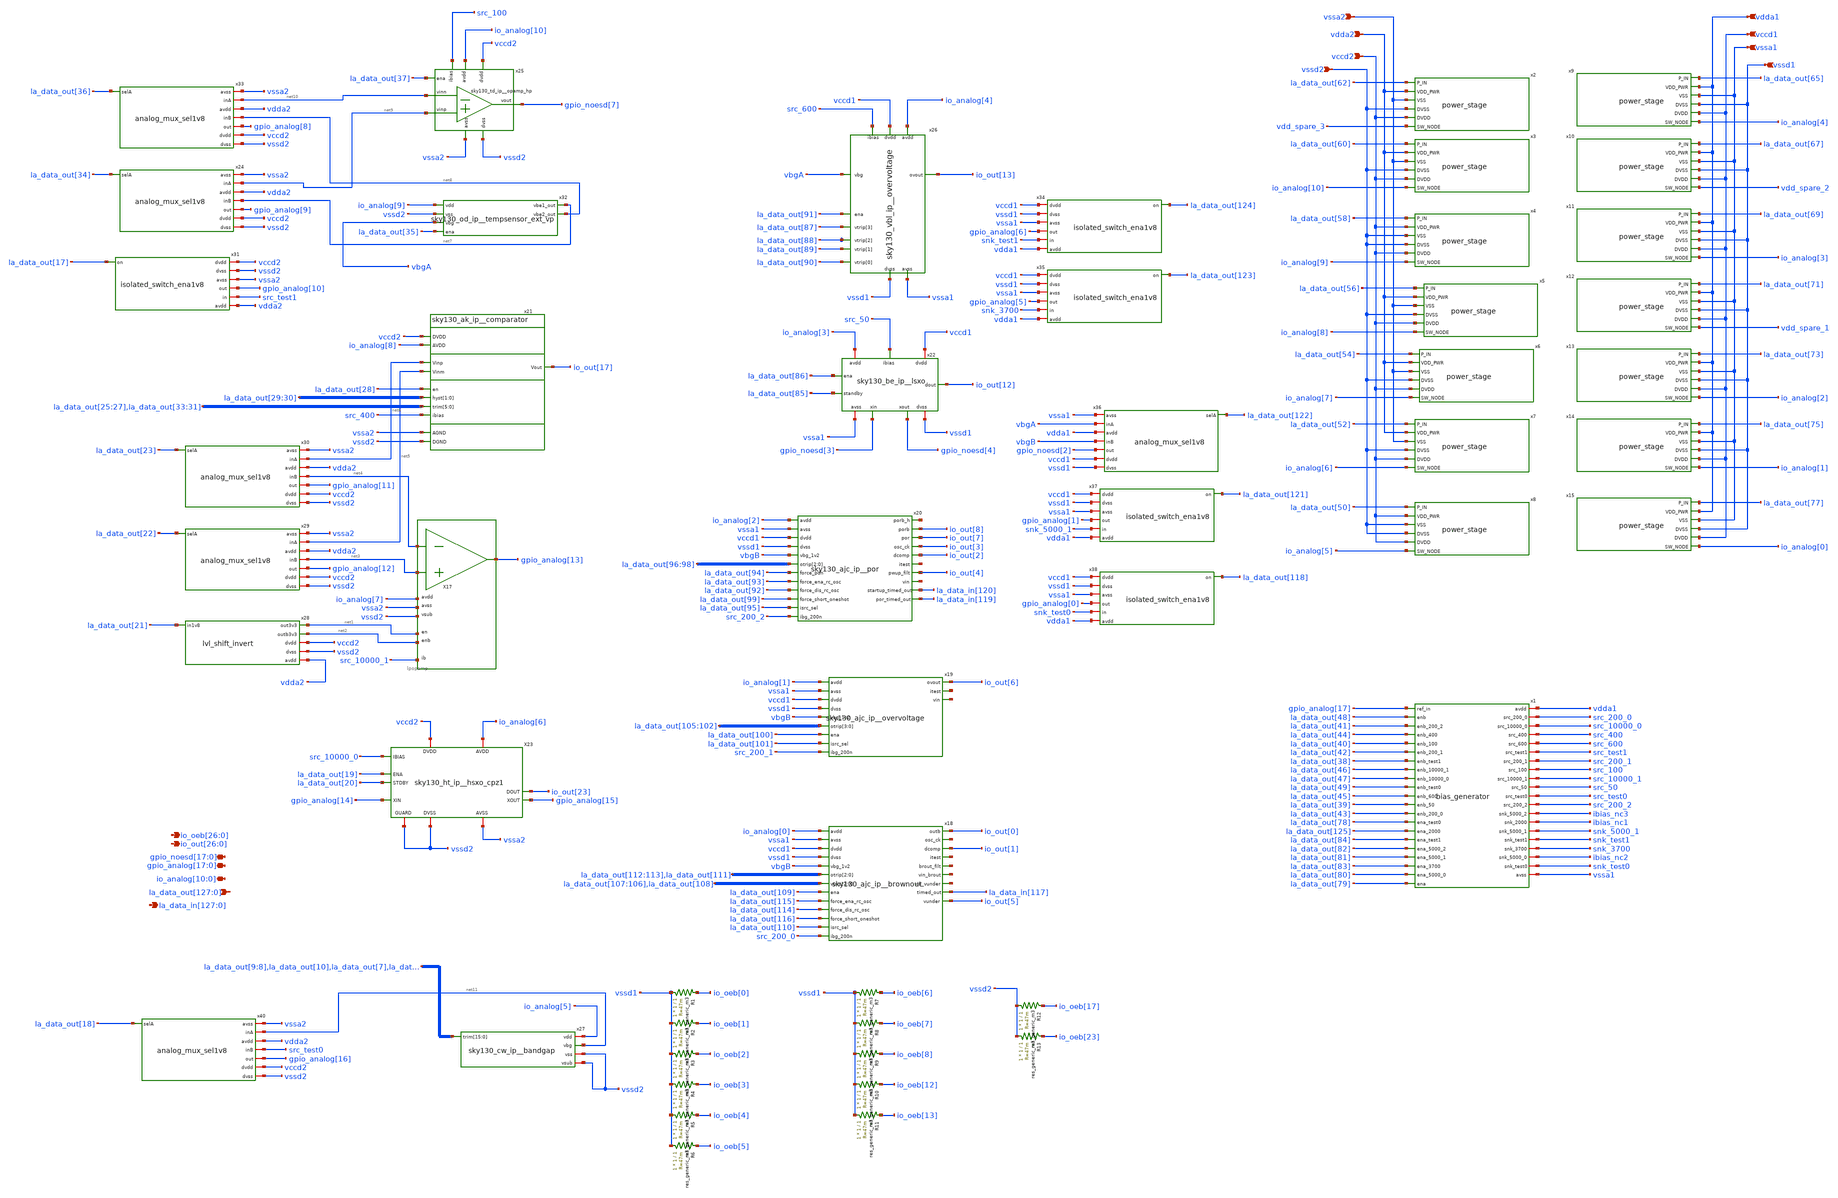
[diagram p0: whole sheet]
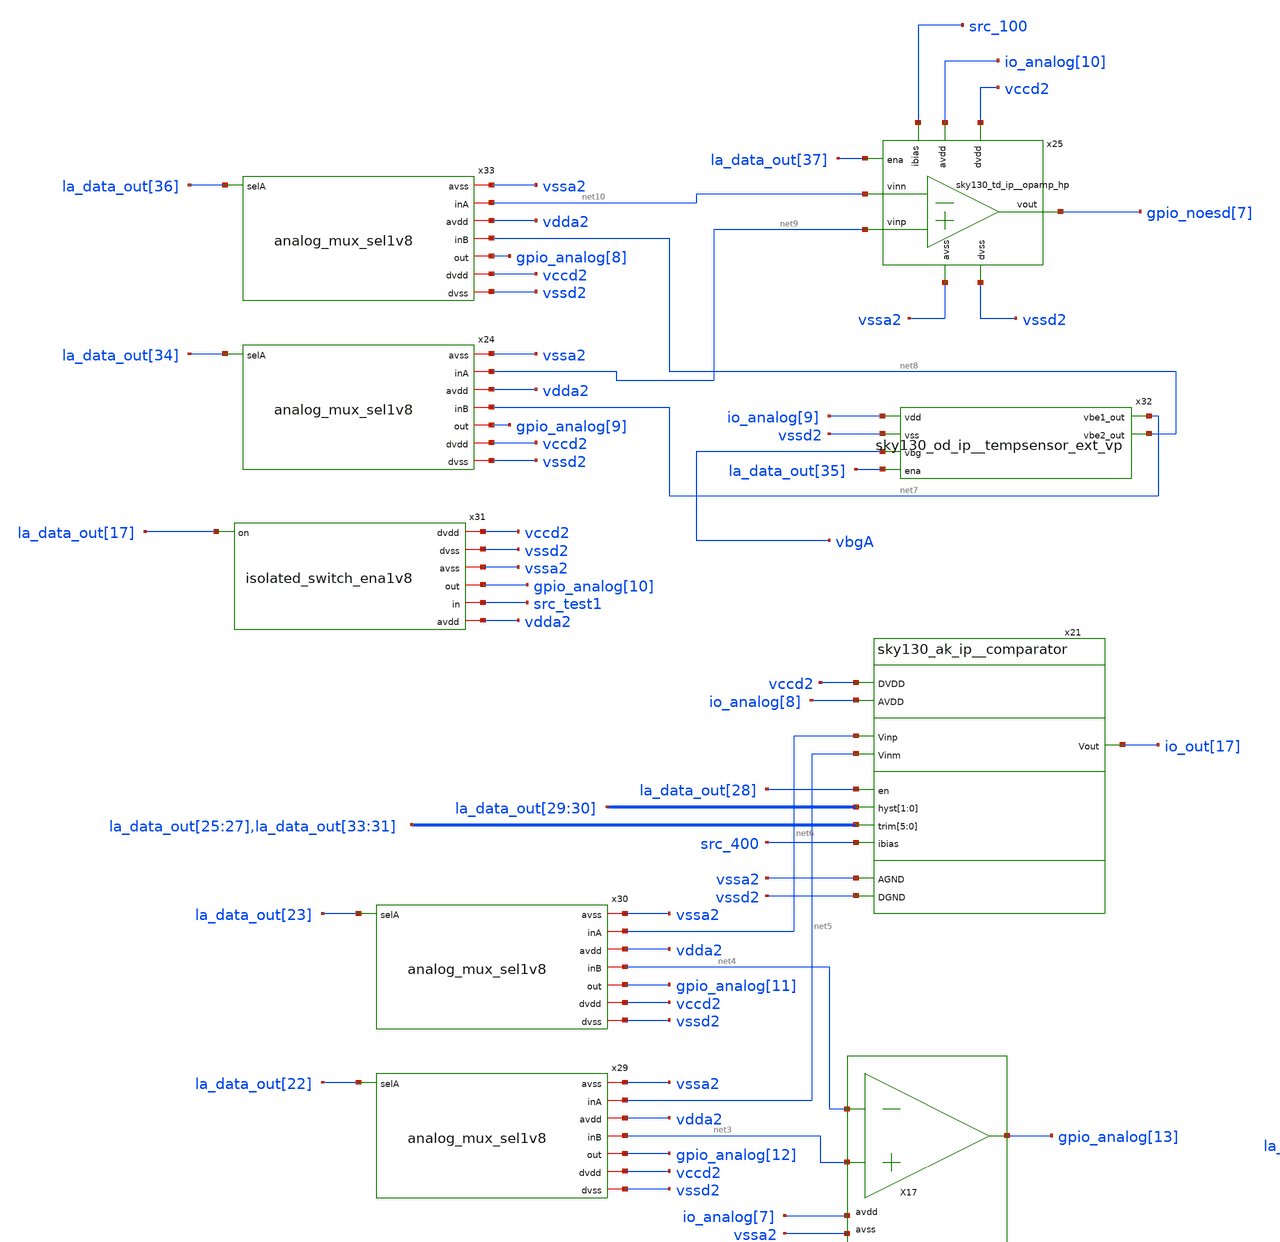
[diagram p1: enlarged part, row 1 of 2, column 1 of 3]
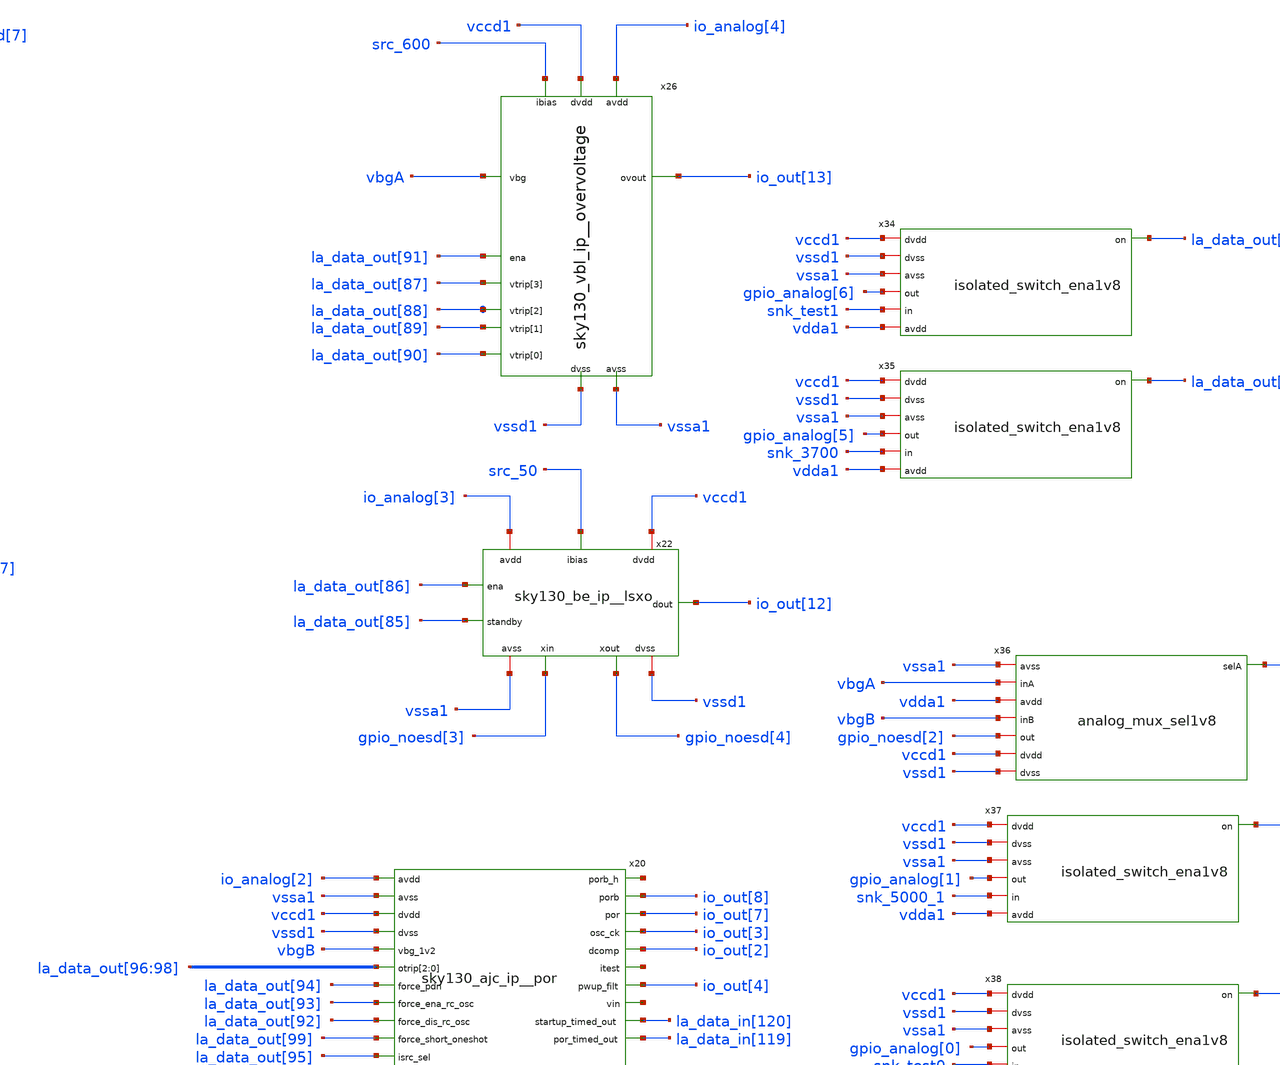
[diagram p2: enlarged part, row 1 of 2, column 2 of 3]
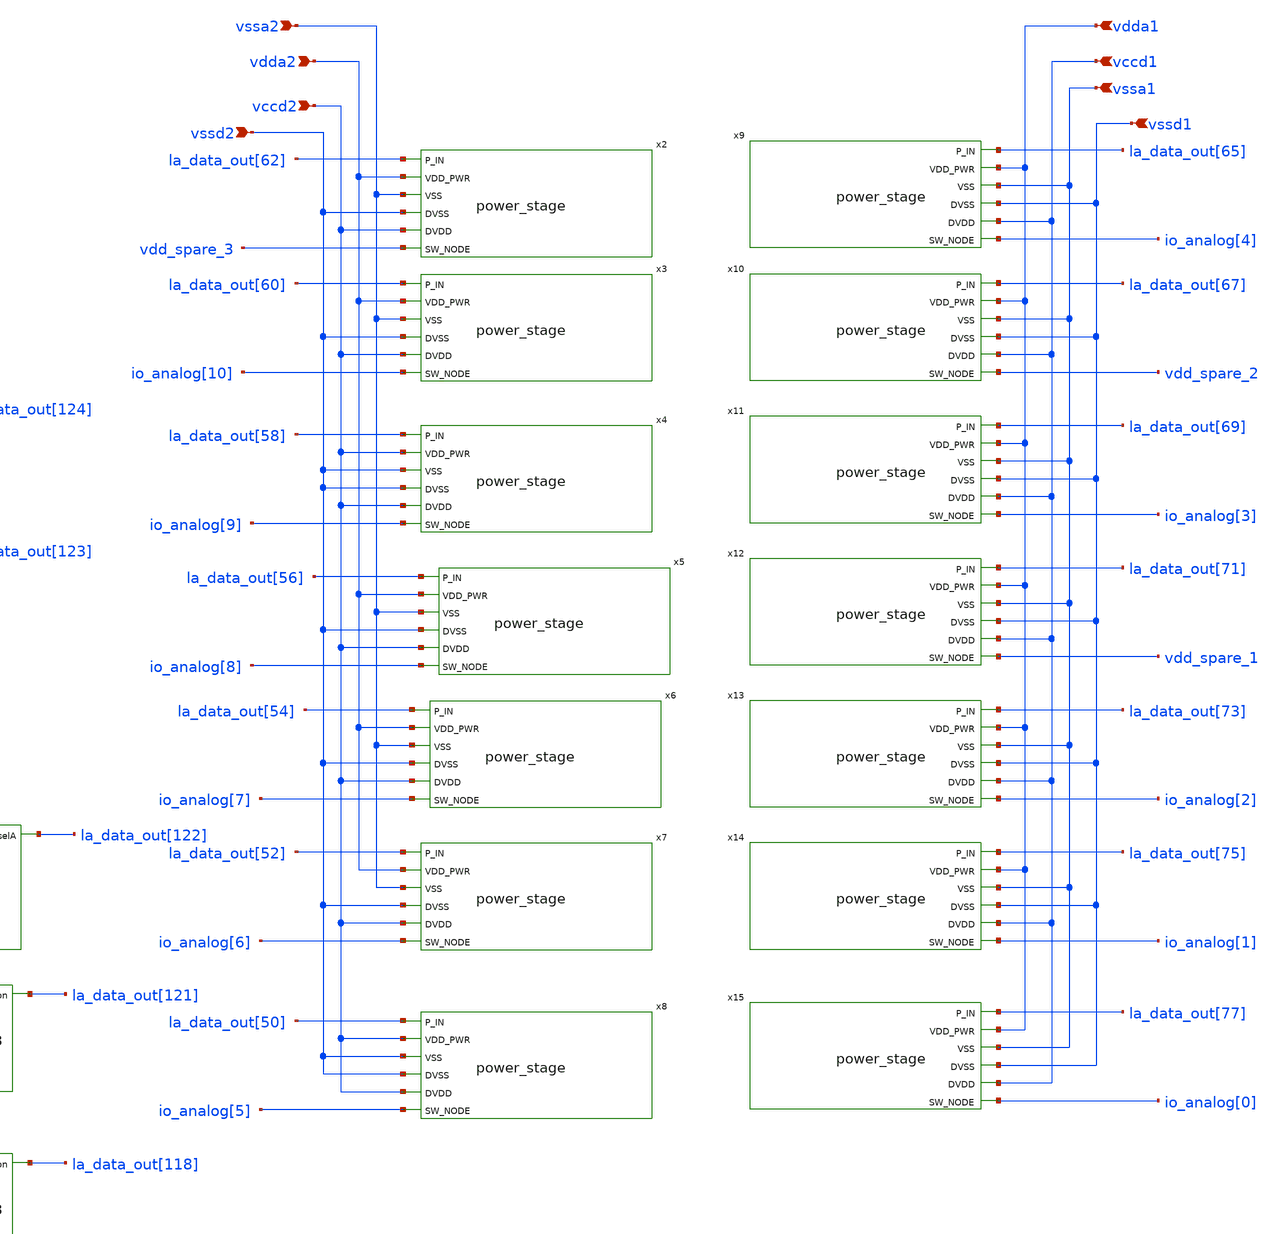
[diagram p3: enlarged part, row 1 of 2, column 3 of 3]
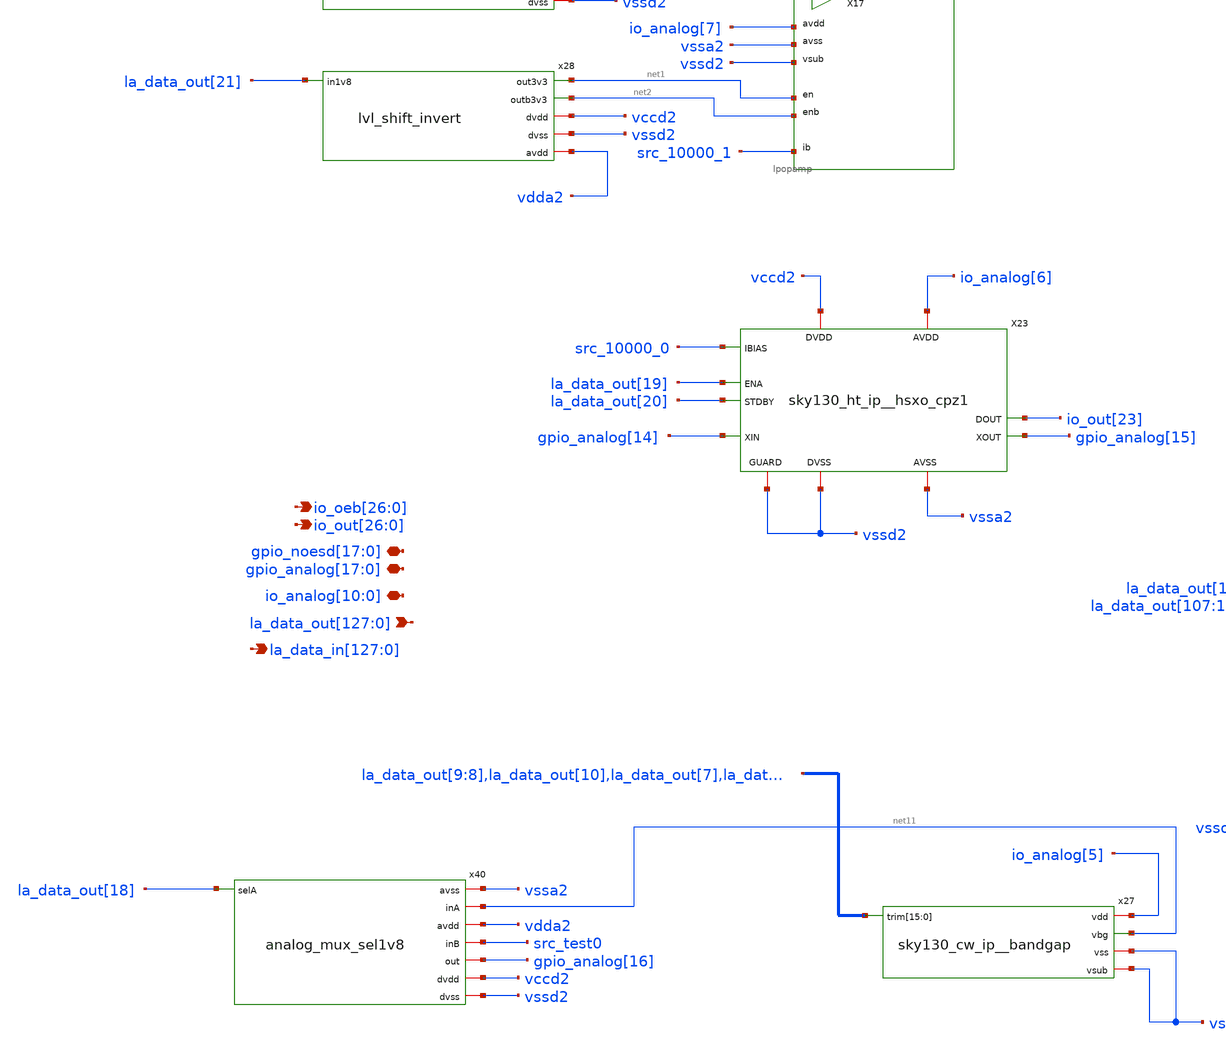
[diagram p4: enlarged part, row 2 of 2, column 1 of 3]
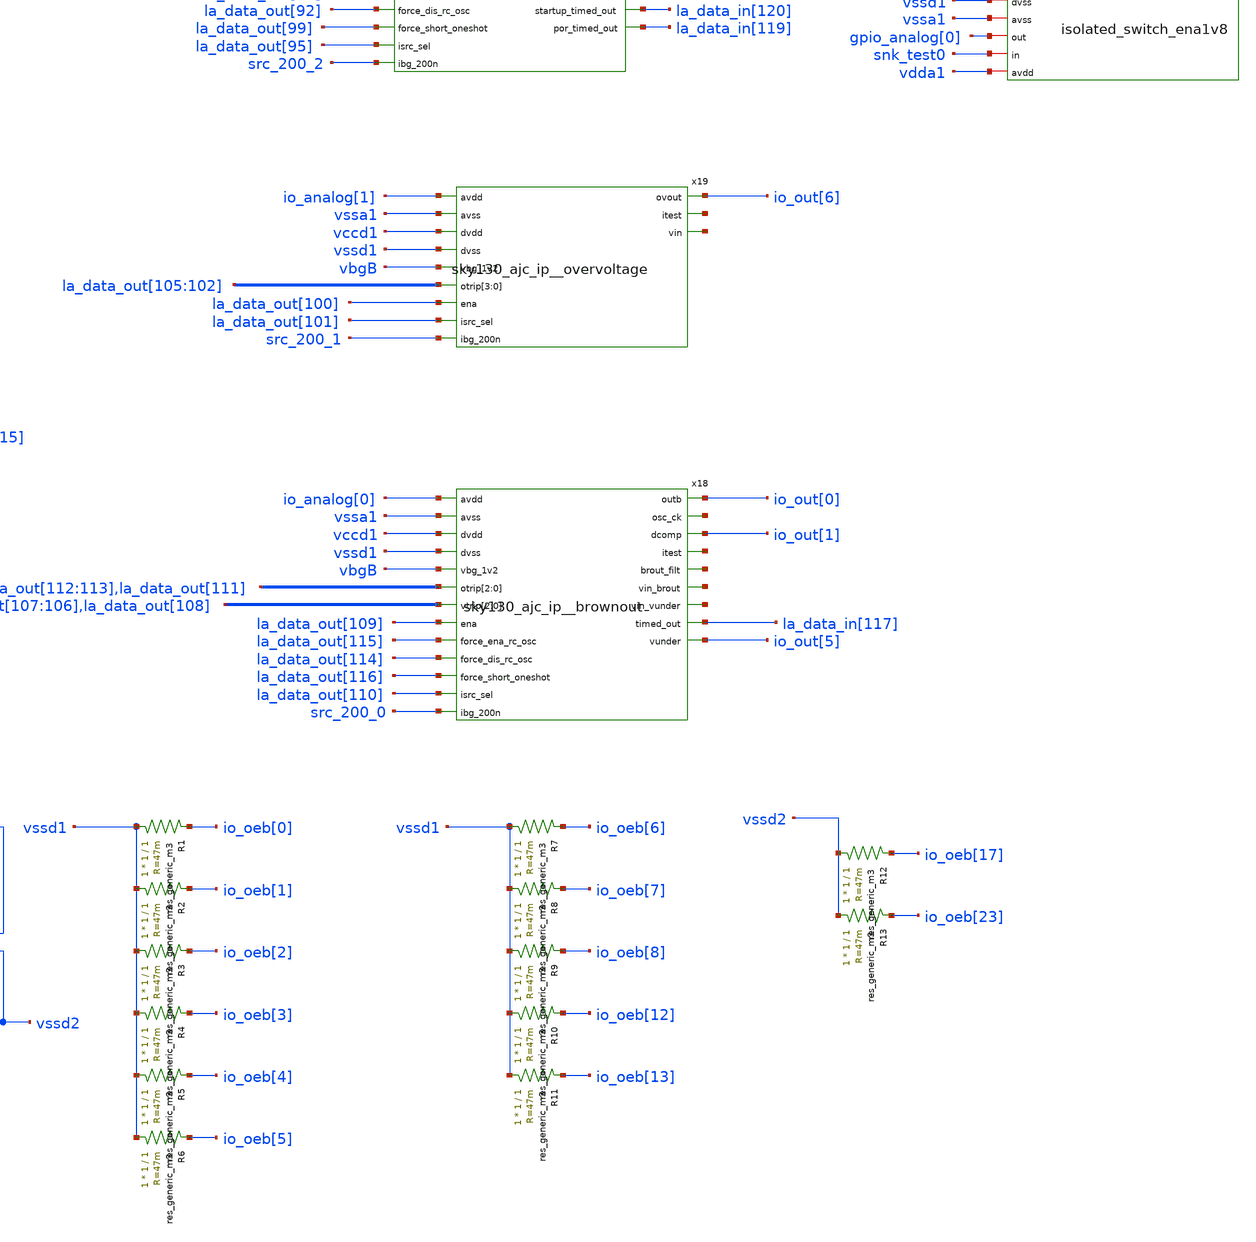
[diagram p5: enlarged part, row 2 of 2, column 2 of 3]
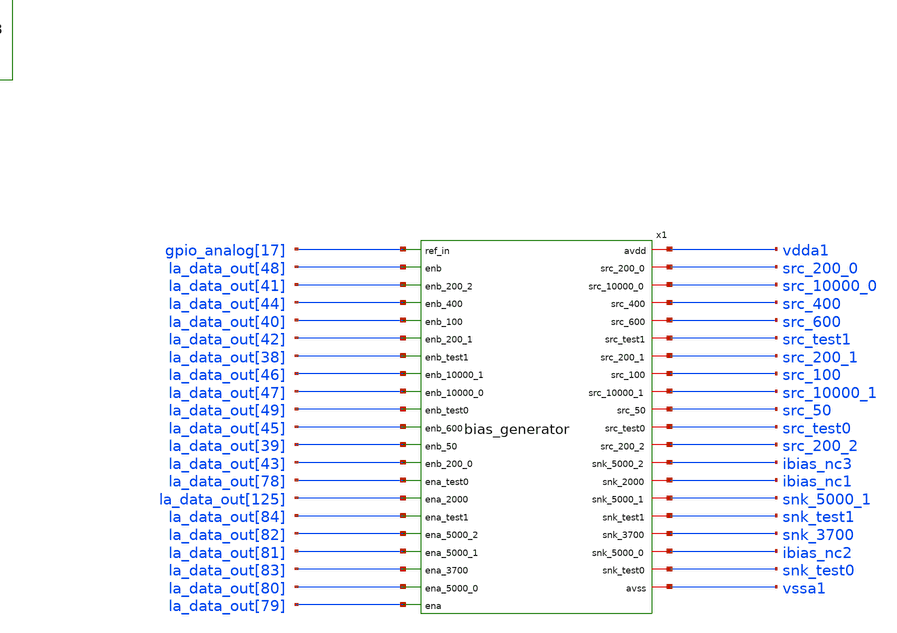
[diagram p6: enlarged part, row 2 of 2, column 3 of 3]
** sch_path: xschem/chipalooza_testchip1.sch
**.subckt chipalooza_testchip1 vdda1 vssa1 vccd2 vdda2 vssa2
*+ gpio_noesd[17],gpio_noesd[16],gpio_noesd[15],gpio_noesd[14],gpio_noesd[13],gpio_noesd[12],gpio_noesd[11],gpio_noesd[10],gpio_noesd[9],gpio_noesd[8],gpio_noesd[7],gpio_noesd[6],gpio_noesd[5],gpio_noesd[4],gpio_noesd[3],gpio_noesd[2],gpio_noesd[1],gpio_noesd[0]
*+ gpio_analog[17],gpio_analog[16],gpio_analog[15],gpio_analog[14],gpio_analog[13],gpio_analog[12],gpio_analog[11],gpio_analog[10],gpio_analog[9],gpio_analog[8],gpio_analog[7],gpio_analog[6],gpio_analog[5],gpio_analog[4],gpio_analog[3],gpio_analog[2],gpio_analog[1],gpio_analog[0]
*+ la_data_out[127],la_data_out[126],la_data_out[125],la_data_out[124],la_data_out[123],la_data_out[122],la_data_out[121],la_data_out[120],la_data_out[119],la_data_out[118],la_data_out[117],la_data_out[116],la_data_out[115],la_data_out[114],la_data_out[113],la_data_out[112],la_data_out[111],la_data_out[110],la_data_out[109],la_data_out[108],la_data_out[107],la_data_out[106],la_data_out[105],la_data_out[104],la_data_out[103],la_data_out[102],la_data_out[101],la_data_out[100],la_data_out[99],la_data_out[98],la_data_out[97],la_data_out[96],la_data_out[95],la_data_out[94],la_data_out[93],la_data_out[92],la_data_out[91],la_data_out[90],la_data_out[89],la_data_out[88],la_data_out[87],la_data_out[86],la_data_out[85],la_data_out[84],la_data_out[83],la_data_out[82],la_data_out[81],la_data_out[80],la_data_out[79],la_data_out[78],la_data_out[77],la_data_out[76],la_data_out[75],la_data_out[74],la_data_out[73],la_data_out[72],la_data_out[71],la_data_out[70],la_data_out[69],la_data_out[68],la_data_out[67],la_data_out[66],la_data_out[65],la_data_out[64],la_data_out[63],la_data_out[62],la_data_out[61],la_data_out[60],la_data_out[59],la_data_out[58],la_data_out[57],la_data_out[56],la_data_out[55],la_data_out[54],la_data_out[53],la_data_out[52],la_data_out[51],la_data_out[50],la_data_out[49],la_data_out[48],la_data_out[47],la_data_out[46],la_data_out[45],la_data_out[44],la_data_out[43],la_data_out[42],la_data_out[41],la_data_out[40],la_data_out[39],la_data_out[38],la_data_out[37],la_data_out[36],la_data_out[35],la_data_out[34],la_data_out[33],la_data_out[32],la_data_out[31],la_data_out[30],la_data_out[29],la_data_out[28],la_data_out[27],la_data_out[26],la_data_out[25],la_data_out[24],la_data_out[23],la_data_out[22],la_data_out[21],la_data_out[20],la_data_out[19],la_data_out[18],la_data_out[17],la_data_out[16],la_data_out[15],la_data_out[14],la_data_out[13],la_data_out[12],la_data_out[11],la_data_out[10],la_data_out[9],la_data_out[8],la_data_out[7],la_data_out[6],la_data_out[5],la_data_out[4],la_data_out[3],la_data_out[2],la_data_out[1],la_data_out[0]
*+ io_out[26],io_out[25],io_out[24],io_out[23],io_out[22],io_out[21],io_out[20],io_out[19],io_out[18],io_out[17],io_out[16],io_out[15],io_out[14],io_out[13],io_out[12],io_out[11],io_out[10],io_out[9],io_out[8],io_out[7],io_out[6],io_out[5],io_out[4],io_out[3],io_out[2],io_out[1],io_out[0]
*+ la_data_in[127],la_data_in[126],la_data_in[125],la_data_in[124],la_data_in[123],la_data_in[122],la_data_in[121],la_data_in[120],la_data_in[119],la_data_in[118],la_data_in[117],la_data_in[116],la_data_in[115],la_data_in[114],la_data_in[113],la_data_in[112],la_data_in[111],la_data_in[110],la_data_in[109],la_data_in[108],la_data_in[107],la_data_in[106],la_data_in[105],la_data_in[104],la_data_in[103],la_data_in[102],la_data_in[101],la_data_in[100],la_data_in[99],la_data_in[98],la_data_in[97],la_data_in[96],la_data_in[95],la_data_in[94],la_data_in[93],la_data_in[92],la_data_in[91],la_data_in[90],la_data_in[89],la_data_in[88],la_data_in[87],la_data_in[86],la_data_in[85],la_data_in[84],la_data_in[83],la_data_in[82],la_data_in[81],la_data_in[80],la_data_in[79],la_data_in[78],la_data_in[77],la_data_in[76],la_data_in[75],la_data_in[74],la_data_in[73],la_data_in[72],la_data_in[71],la_data_in[70],la_data_in[69],la_data_in[68],la_data_in[67],la_data_in[66],la_data_in[65],la_data_in[64],la_data_in[63],la_data_in[62],la_data_in[61],la_data_in[60],la_data_in[59],la_data_in[58],la_data_in[57],la_data_in[56],la_data_in[55],la_data_in[54],la_data_in[53],la_data_in[52],la_data_in[51],la_data_in[50],la_data_in[49],la_data_in[48],la_data_in[47],la_data_in[46],la_data_in[45],la_data_in[44],la_data_in[43],la_data_in[42],la_data_in[41],la_data_in[40],la_data_in[39],la_data_in[38],la_data_in[37],la_data_in[36],la_data_in[35],la_data_in[34],la_data_in[33],la_data_in[32],la_data_in[31],la_data_in[30],la_data_in[29],la_data_in[28],la_data_in[27],la_data_in[26],la_data_in[25],la_data_in[24],la_data_in[23],la_data_in[22],la_data_in[21],la_data_in[20],la_data_in[19],la_data_in[18],la_data_in[17],la_data_in[16],la_data_in[15],la_data_in[14],la_data_in[13],la_data_in[12],la_data_in[11],la_data_in[10],la_data_in[9],la_data_in[8],la_data_in[7],la_data_in[6],la_data_in[5],la_data_in[4],la_data_in[3],la_data_in[2],la_data_in[1],la_data_in[0]
*+ io_oeb[26],io_oeb[25],io_oeb[24],io_oeb[23],io_oeb[22],io_oeb[21],io_oeb[20],io_oeb[19],io_oeb[18],io_oeb[17],io_oeb[16],io_oeb[15],io_oeb[14],io_oeb[13],io_oeb[12],io_oeb[11],io_oeb[10],io_oeb[9],io_oeb[8],io_oeb[7],io_oeb[6],io_oeb[5],io_oeb[4],io_oeb[3],io_oeb[2],io_oeb[1],io_oeb[0]
*+ io_analog[10],io_analog[9],io_analog[8],io_analog[7],io_analog[6],io_analog[5],io_analog[4],io_analog[3],io_analog[2],io_analog[1],io_analog[0] vssd2 vssd1 vccd1
*.ipin vdda1
*.ipin vssa1
*.ipin vccd2
*.ipin vdda2
*.ipin vssa2
*.iopin
*+ gpio_noesd[17],gpio_noesd[16],gpio_noesd[15],gpio_noesd[14],gpio_noesd[13],gpio_noesd[12],gpio_noesd[11],gpio_noesd[10],gpio_noesd[9],gpio_noesd[8],gpio_noesd[7],gpio_noesd[6],gpio_noesd[5],gpio_noesd[4],gpio_noesd[3],gpio_noesd[2],gpio_noesd[1],gpio_noesd[0]
*.iopin
*+ gpio_analog[17],gpio_analog[16],gpio_analog[15],gpio_analog[14],gpio_analog[13],gpio_analog[12],gpio_analog[11],gpio_analog[10],gpio_analog[9],gpio_analog[8],gpio_analog[7],gpio_analog[6],gpio_analog[5],gpio_analog[4],gpio_analog[3],gpio_analog[2],gpio_analog[1],gpio_analog[0]
*.ipin
*+ la_data_out[127],la_data_out[126],la_data_out[125],la_data_out[124],la_data_out[123],la_data_out[122],la_data_out[121],la_data_out[120],la_data_out[119],la_data_out[118],la_data_out[117],la_data_out[116],la_data_out[115],la_data_out[114],la_data_out[113],la_data_out[112],la_data_out[111],la_data_out[110],la_data_out[109],la_data_out[108],la_data_out[107],la_data_out[106],la_data_out[105],la_data_out[104],la_data_out[103],la_data_out[102],la_data_out[101],la_data_out[100],la_data_out[99],la_data_out[98],la_data_out[97],la_data_out[96],la_data_out[95],la_data_out[94],la_data_out[93],la_data_out[92],la_data_out[91],la_data_out[90],la_data_out[89],la_data_out[88],la_data_out[87],la_data_out[86],la_data_out[85],la_data_out[84],la_data_out[83],la_data_out[82],la_data_out[81],la_data_out[80],la_data_out[79],la_data_out[78],la_data_out[77],la_data_out[76],la_data_out[75],la_data_out[74],la_data_out[73],la_data_out[72],la_data_out[71],la_data_out[70],la_data_out[69],la_data_out[68],la_data_out[67],la_data_out[66],la_data_out[65],la_data_out[64],la_data_out[63],la_data_out[62],la_data_out[61],la_data_out[60],la_data_out[59],la_data_out[58],la_data_out[57],la_data_out[56],la_data_out[55],la_data_out[54],la_data_out[53],la_data_out[52],la_data_out[51],la_data_out[50],la_data_out[49],la_data_out[48],la_data_out[47],la_data_out[46],la_data_out[45],la_data_out[44],la_data_out[43],la_data_out[42],la_data_out[41],la_data_out[40],la_data_out[39],la_data_out[38],la_data_out[37],la_data_out[36],la_data_out[35],la_data_out[34],la_data_out[33],la_data_out[32],la_data_out[31],la_data_out[30],la_data_out[29],la_data_out[28],la_data_out[27],la_data_out[26],la_data_out[25],la_data_out[24],la_data_out[23],la_data_out[22],la_data_out[21],la_data_out[20],la_data_out[19],la_data_out[18],la_data_out[17],la_data_out[16],la_data_out[15],la_data_out[14],la_data_out[13],la_data_out[12],la_data_out[11],la_data_out[10],la_data_out[9],la_data_out[8],la_data_out[7],la_data_out[6],la_data_out[5],la_data_out[4],la_data_out[3],la_data_out[2],la_data_out[1],la_data_out[0]
*.opin
*+ io_out[26],io_out[25],io_out[24],io_out[23],io_out[22],io_out[21],io_out[20],io_out[19],io_out[18],io_out[17],io_out[16],io_out[15],io_out[14],io_out[13],io_out[12],io_out[11],io_out[10],io_out[9],io_out[8],io_out[7],io_out[6],io_out[5],io_out[4],io_out[3],io_out[2],io_out[1],io_out[0]
*.opin
*+ la_data_in[127],la_data_in[126],la_data_in[125],la_data_in[124],la_data_in[123],la_data_in[122],la_data_in[121],la_data_in[120],la_data_in[119],la_data_in[118],la_data_in[117],la_data_in[116],la_data_in[115],la_data_in[114],la_data_in[113],la_data_in[112],la_data_in[111],la_data_in[110],la_data_in[109],la_data_in[108],la_data_in[107],la_data_in[106],la_data_in[105],la_data_in[104],la_data_in[103],la_data_in[102],la_data_in[101],la_data_in[100],la_data_in[99],la_data_in[98],la_data_in[97],la_data_in[96],la_data_in[95],la_data_in[94],la_data_in[93],la_data_in[92],la_data_in[91],la_data_in[90],la_data_in[89],la_data_in[88],la_data_in[87],la_data_in[86],la_data_in[85],la_data_in[84],la_data_in[83],la_data_in[82],la_data_in[81],la_data_in[80],la_data_in[79],la_data_in[78],la_data_in[77],la_data_in[76],la_data_in[75],la_data_in[74],la_data_in[73],la_data_in[72],la_data_in[71],la_data_in[70],la_data_in[69],la_data_in[68],la_data_in[67],la_data_in[66],la_data_in[65],la_data_in[64],la_data_in[63],la_data_in[62],la_data_in[61],la_data_in[60],la_data_in[59],la_data_in[58],la_data_in[57],la_data_in[56],la_data_in[55],la_data_in[54],la_data_in[53],la_data_in[52],la_data_in[51],la_data_in[50],la_data_in[49],la_data_in[48],la_data_in[47],la_data_in[46],la_data_in[45],la_data_in[44],la_data_in[43],la_data_in[42],la_data_in[41],la_data_in[40],la_data_in[39],la_data_in[38],la_data_in[37],la_data_in[36],la_data_in[35],la_data_in[34],la_data_in[33],la_data_in[32],la_data_in[31],la_data_in[30],la_data_in[29],la_data_in[28],la_data_in[27],la_data_in[26],la_data_in[25],la_data_in[24],la_data_in[23],la_data_in[22],la_data_in[21],la_data_in[20],la_data_in[19],la_data_in[18],la_data_in[17],la_data_in[16],la_data_in[15],la_data_in[14],la_data_in[13],la_data_in[12],la_data_in[11],la_data_in[10],la_data_in[9],la_data_in[8],la_data_in[7],la_data_in[6],la_data_in[5],la_data_in[4],la_data_in[3],la_data_in[2],la_data_in[1],la_data_in[0]
*.opin
*+ io_oeb[26],io_oeb[25],io_oeb[24],io_oeb[23],io_oeb[22],io_oeb[21],io_oeb[20],io_oeb[19],io_oeb[18],io_oeb[17],io_oeb[16],io_oeb[15],io_oeb[14],io_oeb[13],io_oeb[12],io_oeb[11],io_oeb[10],io_oeb[9],io_oeb[8],io_oeb[7],io_oeb[6],io_oeb[5],io_oeb[4],io_oeb[3],io_oeb[2],io_oeb[1],io_oeb[0]
*.iopin
*+ io_analog[10],io_analog[9],io_analog[8],io_analog[7],io_analog[6],io_analog[5],io_analog[4],io_analog[3],io_analog[2],io_analog[1],io_analog[0]
*.ipin vssd2
*.ipin vssd1
*.ipin vccd1
x1 vdda1 gpio_analog[17] la_data_out[48] la_data_out[41] la_data_out[44] la_data_out[40]
+ la_data_out[42] la_data_out[38] la_data_out[46] la_data_out[47] la_data_out[49] la_data_out[45] la_data_out[39]
+ la_data_out[43] src_200_0 src_10000_0 src_400 src_600 src_test1 src_200_1 src_100 src_10000_1 src_50 src_test0
+ src_200_2 la_data_out[78] la_data_out[125] la_data_out[84] la_data_out[82] la_data_out[81] la_data_out[83]
+ la_data_out[80] ibias_nc3 ibias_nc1 snk_5000_1 snk_test1 snk_3700 ibias_nc2 snk_test0 la_data_out[79] vssa1
+ bias_generator
x2 la_data_out[62] vdda2 vssa2 vssd2 vccd2 vdd_spare_3 power_stage
x3 la_data_out[60] vdda2 vssa2 vssd2 vccd2 io_analog[10] power_stage
x4 la_data_out[58] vccd2 vssd2 vssd2 vccd2 io_analog[9] power_stage
x5 la_data_out[56] vdda2 vssa2 vssd2 vccd2 io_analog[8] power_stage
x6 la_data_out[54] vdda2 vssa2 vssd2 vccd2 io_analog[7] power_stage
x7 la_data_out[52] vdda2 vssa2 vssd2 vccd2 io_analog[6] power_stage
x8 la_data_out[50] vccd2 vssd2 vssd2 vccd2 io_analog[5] power_stage
x9 la_data_out[65] vdda1 vssa1 vssd1 vccd1 io_analog[4] power_stage
x10 la_data_out[67] vdda1 vssa1 vssd1 vccd1 vdd_spare_2 power_stage
x11 la_data_out[69] vdda1 vssa1 vssd1 vccd1 io_analog[3] power_stage
x12 la_data_out[71] vdda1 vssa1 vssd1 vccd1 vdd_spare_1 power_stage
x13 la_data_out[73] vdda1 vssa1 vssd1 vccd1 io_analog[2] power_stage
x14 la_data_out[75] vdda1 vssa1 vssd1 vccd1 io_analog[1] power_stage
x15 la_data_out[77] vdda1 vssa1 vssd1 vccd1 io_analog[0] power_stage
X17 net4 gpio_analog[13] src_10000_1 vssd2 vssa2 io_analog[7] net2 net1 net3 lpopamp
x18 io_analog[0] vssa1 io_out[0] vccd1 net12 vssd1 io_out[1] vbgB la_data_out[112] la_data_out[113]
+ la_data_out[111] net13 net14 la_data_out[107] la_data_out[106] la_data_out[108] net15 la_data_out[109]
+ la_data_out[115] net16 la_data_out[114] la_data_in[117] io_out[5] la_data_out[116] la_data_out[110] src_200_0
+ sky130_ajc_ip__brownout
x19 io_analog[1] vssa1 vccd1 vssd1 vbgB io_out[6] net17 la_data_out[105] la_data_out[104]
+ la_data_out[103] la_data_out[102] net18 la_data_out[100] la_data_out[101] src_200_1 sky130_ajc_ip__overvoltage
x20 io_analog[2] net19 io_out[8] vssa1 vccd1 io_out[7] vssd1 io_out[3] vbgB io_out[2]
+ la_data_out[96] la_data_out[97] la_data_out[98] net20 la_data_out[94] io_out[4] net21 la_data_out[93]
+ la_data_out[92] la_data_in[120] la_data_in[119] la_data_out[99] la_data_out[95] src_200_2 sky130_ajc_ip__por
x21 vccd2 io_analog[8] vssa2 net6 io_out[17] net5 la_data_out[28] la_data_out[29] la_data_out[30]
+ la_data_out[25] la_data_out[26] la_data_out[27] la_data_out[33] la_data_out[32] la_data_out[31] src_400 vssd2
+ sky130_ak_ip__comparator
x22 io_analog[3] vssa1 vccd1 vssd1 src_50 la_data_out[86] la_data_out[85] io_out[12] gpio_noesd[3]
+ gpio_noesd[4] sky130_be_ip__lsxo
X23 gpio_analog[15] gpio_analog[14] la_data_out[19] la_data_out[20] io_out[23] io_analog[6] vccd2
+ vssa2 vssd2 src_10000_0 vssd2 sky130_ht_ip__hsxo_cpz1
x25 io_analog[10] gpio_noesd[7] src_100 net10 net9 vssa2 vccd2 vssd2 la_data_out[37]
+ sky130_td_ip__opamp_hp
x26 io_analog[4] vccd1 la_data_out[91] la_data_out[87] src_600 la_data_out[88] io_out[13] vbgA
+ la_data_out[89] la_data_out[90] vssd1 vssa1 sky130_vbl_ip__overvoltage
x28 la_data_out[21] net1 net2 vccd2 vssd2 vdda2 lvl_shift_invert
x29 vssa2 la_data_out[22] net5 vdda2 net3 gpio_analog[12] vccd2 vssd2 analog_mux_sel1v8
x30 vssa2 la_data_out[23] net6 vdda2 net4 gpio_analog[11] vccd2 vssd2 analog_mux_sel1v8
x31 vssa2 la_data_out[17] gpio_analog[10] src_test1 vdda2 vccd2 vssd2 isolated_switch_ena1v8
x32 net7 io_analog[9] vssd2 vbgA la_data_out[35] net8 sky130_od_ip__tempsensor_ext_vp
x24 vssa2 la_data_out[34] net9 vdda2 net7 gpio_analog[9] vccd2 vssd2 analog_mux_sel1v8
x33 vssa2 la_data_out[36] net10 vdda2 net8 gpio_analog[8] vccd2 vssd2 analog_mux_sel1v8
x34 vssa1 la_data_out[124] gpio_analog[6] snk_test1 vdda1 vccd1 vssd1 isolated_switch_ena1v8
x35 vssa1 la_data_out[123] gpio_analog[5] snk_3700 vdda1 vccd1 vssd1 isolated_switch_ena1v8
x36 vssa1 la_data_out[122] vbgA vdda1 vbgB gpio_noesd[2] vccd1 vssd1 analog_mux_sel1v8
x37 vssa1 la_data_out[121] gpio_analog[1] snk_5000_1 vdda1 vccd1 vssd1 isolated_switch_ena1v8
x38 vssa1 la_data_out[118] gpio_analog[0] snk_test0 vdda1 vccd1 vssd1 isolated_switch_ena1v8
x40 vssa2 la_data_out[18] net11 vdda2 src_test0 gpio_analog[16] vccd2 vssd2 analog_mux_sel1v8
R1 vssd1 io_oeb[0] sky130_fd_pr__res_generic_m3 W=1 L=1 m=1
R2 vssd1 io_oeb[1] sky130_fd_pr__res_generic_m3 W=1 L=1 m=1
R3 vssd1 io_oeb[2] sky130_fd_pr__res_generic_m3 W=1 L=1 m=1
R4 vssd1 io_oeb[3] sky130_fd_pr__res_generic_m3 W=1 L=1 m=1
R5 vssd1 io_oeb[4] sky130_fd_pr__res_generic_m3 W=1 L=1 m=1
R6 vssd1 io_oeb[5] sky130_fd_pr__res_generic_m3 W=1 L=1 m=1
R7 vssd1 io_oeb[6] sky130_fd_pr__res_generic_m3 W=1 L=1 m=1
R8 vssd1 io_oeb[7] sky130_fd_pr__res_generic_m3 W=1 L=1 m=1
R9 vssd1 io_oeb[8] sky130_fd_pr__res_generic_m3 W=1 L=1 m=1
R10 vssd1 io_oeb[12] sky130_fd_pr__res_generic_m3 W=1 L=1 m=1
R11 vssd1 io_oeb[13] sky130_fd_pr__res_generic_m3 W=1 L=1 m=1
R12 vssd2 io_oeb[17] sky130_fd_pr__res_generic_m3 W=1 L=1 m=1
R13 vssd2 io_oeb[23] sky130_fd_pr__res_generic_m3 W=1 L=1 m=1
x27 io_analog[5] la_data_out[9] la_data_out[8] la_data_out[10] la_data_out[7] la_data_out[11]
+ la_data_out[6] la_data_out[12] la_data_out[5] la_data_out[13] la_data_out[4] la_data_out[14] la_data_out[3]
+ la_data_out[15] la_data_out[2] la_data_out[16] la_data_out[1] net11 vssd2 vssd2 sky130_cw_ip__bandgap
**.ends
.end
